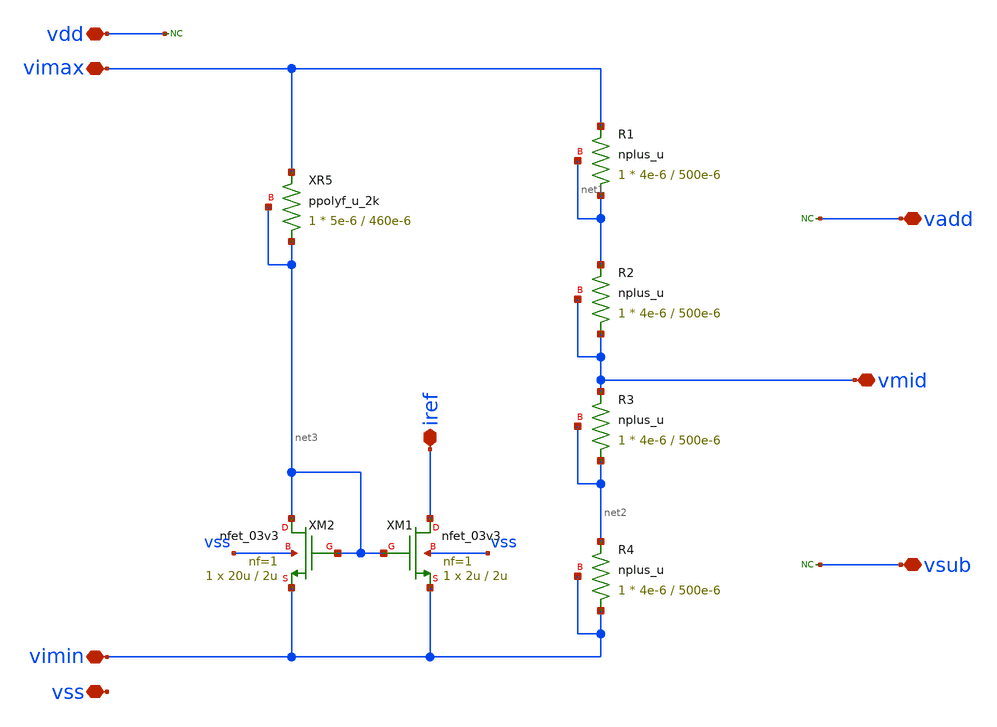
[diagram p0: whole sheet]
** sch_path: General/ADC/Reference/Reference_circuits_v2.sch
**.subckt Reference_circuits_v2 vimax vimin iref vadd vmid vsub vss vdd
*.iopin vimax
*.iopin vimin
*.iopin iref
*.iopin vadd
*.iopin vmid
*.iopin vsub
*.iopin vss
*.iopin vdd
XR1 net1 vimax net1 nplus_u r_width=4e-6 r_length=500e-6 m=1
XR2 vmid net1 vmid nplus_u r_width=4e-6 r_length=500e-6 m=1
XR3 net2 vmid net2 nplus_u r_width=4e-6 r_length=500e-6 m=1
XR4 vimin net2 vimin nplus_u r_width=4e-6 r_length=500e-6 m=1
XM2 net3 net3 vimin vss nfet_03v3 L=2u W=20u nf=1 ad='int((nf+1)/2) * W/nf * 0.18u' as='int((nf+2)/2) * W/nf * 0.18u'
+ pd='2*int((nf+1)/2) * (W/nf + 0.18u)' ps='2*int((nf+2)/2) * (W/nf + 0.18u)' nrd='0.18u / W' nrs='0.18u / W'
+ sa=0 sb=0 sd=0 m=1
XR5 net3 vimax net3 ppolyf_u_2k r_width=5e-6 r_length=460e-6 m=1
XM1 iref net3 vimin vss nfet_03v3 L=2u W=2u nf=1 ad='int((nf+1)/2) * W/nf * 0.18u' as='int((nf+2)/2) * W/nf * 0.18u'
+ pd='2*int((nf+1)/2) * (W/nf + 0.18u)' ps='2*int((nf+2)/2) * (W/nf + 0.18u)' nrd='0.18u / W' nrs='0.18u / W'
+ sa=0 sb=0 sd=0 m=1
* noconn vdd
* noconn vadd
* noconn vsub
**.ends
.end
